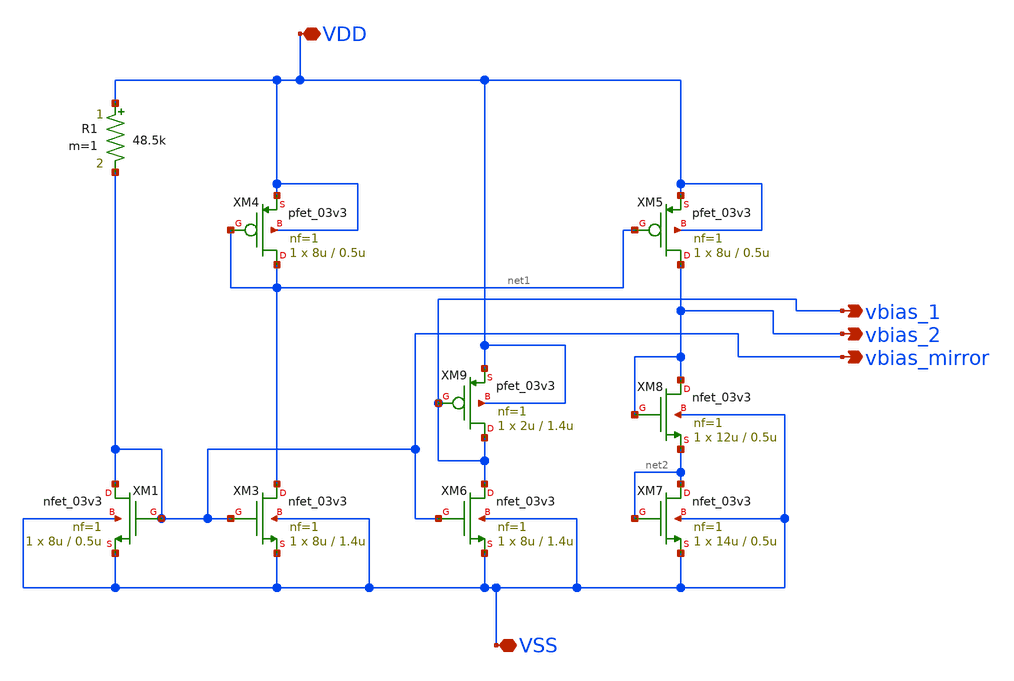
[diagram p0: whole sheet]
** sch_path: xschem/amp_bias.sch
**.subckt amp_bias VDD VSS vbias_1 vbias_2 vbias_mirror
*.iopin VDD
*.iopin VSS
*.opin vbias_1
*.opin vbias_2
*.opin vbias_mirror
R1 VDD vbias_mirror 48.5k m=1
XM1 vbias_mirror vbias_mirror VSS VSS nfet_03v3 L=0.5u W=8u nf=1 ad='int((nf+1)/2) * W/nf * 0.18u' as='int((nf+2)/2) * W/nf * 0.18u'
+ pd='2*int((nf+1)/2) * (W/nf + 0.18u)' ps='2*int((nf+2)/2) * (W/nf + 0.18u)' nrd='0.18u / W' nrs='0.18u / W'
+ sa=0 sb=0 sd=0 m=1 par=1
XM3 net1 vbias_mirror VSS VSS nfet_03v3 L=1.4u W=8u nf=1 ad='int((nf+1)/2) * W/nf * 0.18u' as='int((nf+2)/2) * W/nf * 0.18u'
+ pd='2*int((nf+1)/2) * (W/nf + 0.18u)' ps='2*int((nf+2)/2) * (W/nf + 0.18u)' nrd='0.18u / W' nrs='0.18u / W'
+ sa=0 sb=0 sd=0 m=1 par=1
XM4 net1 net1 VDD VDD pfet_03v3 L=0.5u W=8u nf=1 ad='int((nf+1)/2) * W/nf * 0.18u' as='int((nf+2)/2) * W/nf * 0.18u'
+ pd='2*int((nf+1)/2) * (W/nf + 0.18u)' ps='2*int((nf+2)/2) * (W/nf + 0.18u)' nrd='0.18u / W' nrs='0.18u / W'
+ sa=0 sb=0 sd=0 m=1
XM5 vbias_2 net1 VDD VDD pfet_03v3 L=0.5u W=8u nf=1 ad='int((nf+1)/2) * W/nf * 0.18u' as='int((nf+2)/2) * W/nf * 0.18u'
+ pd='2*int((nf+1)/2) * (W/nf + 0.18u)' ps='2*int((nf+2)/2) * (W/nf + 0.18u)' nrd='0.18u / W' nrs='0.18u / W'
+ sa=0 sb=0 sd=0 m=1
XM6 vbias_1 vbias_mirror VSS VSS nfet_03v3 L=1.4u W=8u nf=1 ad='int((nf+1)/2) * W/nf * 0.18u' as='int((nf+2)/2) * W/nf * 0.18u'
+ pd='2*int((nf+1)/2) * (W/nf + 0.18u)' ps='2*int((nf+2)/2) * (W/nf + 0.18u)' nrd='0.18u / W' nrs='0.18u / W'
+ sa=0 sb=0 sd=0 m=1 par=1
XM7 net2 net2 VSS VSS nfet_03v3 L=0.5u W=14u nf=1 ad='int((nf+1)/2) * W/nf * 0.18u' as='int((nf+2)/2) * W/nf * 0.18u'
+ pd='2*int((nf+1)/2) * (W/nf + 0.18u)' ps='2*int((nf+2)/2) * (W/nf + 0.18u)' nrd='0.18u / W' nrs='0.18u / W'
+ sa=0 sb=0 sd=0 m=1 par=1
XM8 vbias_2 vbias_2 net2 VSS nfet_03v3 L=0.5u W=12u nf=1 ad='int((nf+1)/2) * W/nf * 0.18u' as='int((nf+2)/2) * W/nf * 0.18u'
+ pd='2*int((nf+1)/2) * (W/nf + 0.18u)' ps='2*int((nf+2)/2) * (W/nf + 0.18u)' nrd='0.18u / W' nrs='0.18u / W'
+ sa=0 sb=0 sd=0 m=1 par=1
XM9 vbias_1 vbias_1 VDD VDD pfet_03v3 L=1.4u W=2u nf=1 ad='int((nf+1)/2) * W/nf * 0.18u' as='int((nf+2)/2) * W/nf * 0.18u'
+ pd='2*int((nf+1)/2) * (W/nf + 0.18u)' ps='2*int((nf+2)/2) * (W/nf + 0.18u)' nrd='0.18u / W' nrs='0.18u / W'
+ sa=0 sb=0 sd=0 m=1
**.ends
.end
